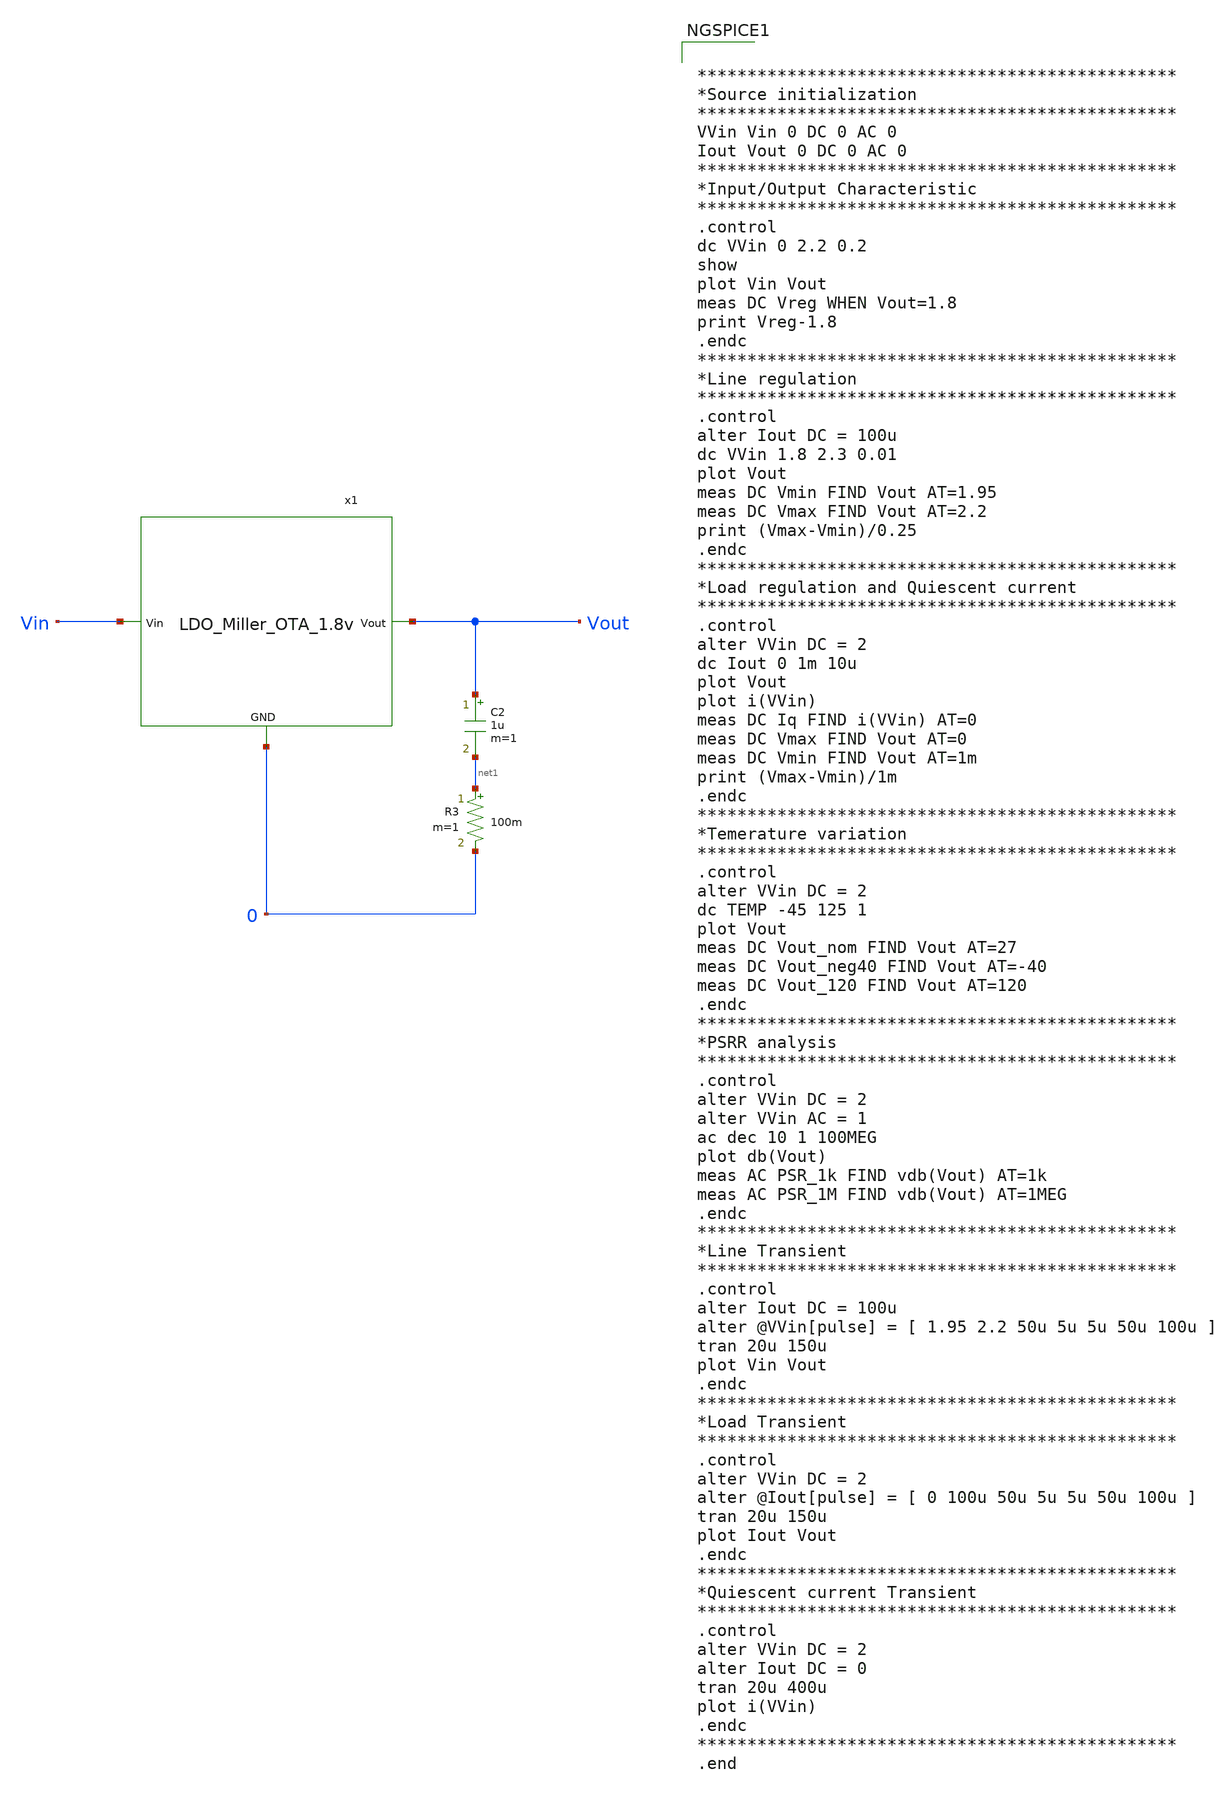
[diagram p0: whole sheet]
** sch_path: Analog_Blocks/LDO/Testbench/LDO_Miller_1.8v_meas.sch
**.subckt LDO_Miller_1.8v_meas
C2 Vout net1 1u m=1
R3 net1 0 100m m=1
x1 Vin Vout 0 LDO_Miller_OTA_1.8v
**** begin user architecture code


************************************************
*Source initialization
************************************************
VVin Vin 0 DC 0 AC 0
Iout Vout 0 DC 0 AC 0
************************************************
*Input/Output Characteristic
************************************************
.control
dc VVin 0 2.2 0.2
show
plot Vin Vout
meas DC Vreg WHEN Vout=1.8
print Vreg-1.8
.endc
************************************************
*Line regulation
************************************************
.control
alter Iout DC = 100u
dc VVin 1.8 2.3 0.01
plot Vout
meas DC Vmin FIND Vout AT=1.95
meas DC Vmax FIND Vout AT=2.2
print (Vmax-Vmin)/0.25
.endc
************************************************
*Load regulation and Quiescent current
************************************************
.control
alter VVin DC = 2
dc Iout 0 1m 10u
plot Vout
plot i(VVin)
meas DC Iq FIND i(VVin) AT=0
meas DC Vmax FIND Vout AT=0
meas DC Vmin FIND Vout AT=1m
print (Vmax-Vmin)/1m
.endc
************************************************
*Temerature variation
************************************************
.control
alter VVin DC = 2
dc TEMP -45 125 1
plot Vout
meas DC Vout_nom FIND Vout AT=27
meas DC Vout_neg40 FIND Vout AT=-40
meas DC Vout_120 FIND Vout AT=120
.endc
************************************************
*PSRR analysis
************************************************
.control
alter VVin DC = 2
alter VVin AC = 1
ac dec 10 1 100MEG
plot db(Vout)
meas AC PSR_1k FIND vdb(Vout) AT=1k
meas AC PSR_1M FIND vdb(Vout) AT=1MEG
.endc
************************************************
*Line Transient
************************************************
.control
alter Iout DC = 100u
alter @VVin[pulse] = [ 1.95 2.2 50u 5u 5u 50u 100u ]
tran 20u 150u
plot Vin Vout
.endc
************************************************
*Load Transient
************************************************
.control
alter VVin DC = 2
alter @Iout[pulse] = [ 0 100u 50u 5u 5u 50u 100u ]
tran 20u 150u
plot Iout Vout
.endc
************************************************
*Quiescent current Transient
************************************************
.control
alter VVin DC = 2
alter Iout DC = 0
tran 20u 400u
plot i(VVin)
.endc
************************************************
.end




.param mc_mm_switch=0
.param mc_pr_switch=0
.include ~/mabrains/Analog_blocks/models/sky130A/libs.ref/sky130_fd_pr/spice/sky130_fd_pr__nfet_01v8__tt.corner.spice
.include ~/mabrains/Analog_blocks/models/sky130A/libs.ref/sky130_fd_pr/spice/sky130_fd_pr__nfet_01v8_lvt__tt.corner.spice
.include ~/mabrains/Analog_blocks/models/sky130A/libs.ref/sky130_fd_pr/spice/sky130_fd_pr__pfet_01v8__tt.corner.spice
.include ~/mabrains/Analog_blocks/models/sky130A/libs.ref/sky130_fd_pr/spice/sky130_fd_pr__nfet_03v3_nvt__tt.corner.spice
.include ~/mabrains/Analog_blocks/models/sky130A/libs.ref/sky130_fd_pr/spice/sky130_fd_pr__nfet_05v0_nvt__tt.corner.spice
.include ~/mabrains/Analog_blocks/models/sky130A/libs.ref/sky130_fd_pr/spice/sky130_fd_pr__esd_nfet_01v8__tt.corner.spice
.include ~/mabrains/Analog_blocks/models/sky130A/libs.ref/sky130_fd_pr/spice/sky130_fd_pr__pfet_01v8_lvt__tt.corner.spice
.include ~/mabrains/Analog_blocks/models/sky130A/libs.ref/sky130_fd_pr/spice/sky130_fd_pr__pfet_01v8_hvt__tt.corner.spice
.include ~/mabrains/Analog_blocks/models/sky130A/libs.ref/sky130_fd_pr/spice/sky130_fd_pr__esd_pfet_g5v0d10v5__tt.corner.spice
.include ~/mabrains/Analog_blocks/models/sky130A/libs.ref/sky130_fd_pr/spice/sky130_fd_pr__pfet_g5v0d10v5__tt.corner.spice
.include ~/mabrains/Analog_blocks/models/sky130A/libs.ref/sky130_fd_pr/spice/sky130_fd_pr__pfet_g5v0d16v0__tt.corner.spice
.include ~/mabrains/Analog_blocks/models/sky130A/libs.ref/sky130_fd_pr/spice/sky130_fd_pr__nfet_g5v0d10v5__tt.corner.spice
.include ~/mabrains/Analog_blocks/models/sky130A/libs.ref/sky130_fd_pr/spice/sky130_fd_pr__nfet_g5v0d16v0__tt_discrete.corner.spice
.include ~/mabrains/Analog_blocks/models/sky130A/libs.ref/sky130_fd_pr/spice/sky130_fd_pr__esd_nfet_g5v0d10v5__tt.corner.spice
.include ~/mabrains/Analog_blocks/models/sky130A/libs.tech/ngspice/corners/tt/nonfet.spice
* Mismatch parameters
.include ~/mabrains/Analog_blocks/models/sky130A/libs.ref/sky130_fd_pr/spice/sky130_fd_pr__nfet_01v8__mismatch.corner.spice
.include ~/mabrains/Analog_blocks/models/sky130A/libs.ref/sky130_fd_pr/spice/sky130_fd_pr__pfet_01v8__mismatch.corner.spice
.include ~/mabrains/Analog_blocks/models/sky130A/libs.ref/sky130_fd_pr/spice/sky130_fd_pr__nfet_01v8_lvt__mismatch.corner.spice
.include ~/mabrains/Analog_blocks/models/sky130A/libs.ref/sky130_fd_pr/spice/sky130_fd_pr__pfet_01v8_lvt__mismatch.corner.spice
.include ~/mabrains/Analog_blocks/models/sky130A/libs.ref/sky130_fd_pr/spice/sky130_fd_pr__pfet_01v8_hvt__mismatch.corner.spice
.include ~/mabrains/Analog_blocks/models/sky130A/libs.ref/sky130_fd_pr/spice/sky130_fd_pr__nfet_g5v0d10v5__mismatch.corner.spice
.include ~/mabrains/Analog_blocks/models/sky130A/libs.ref/sky130_fd_pr/spice/sky130_fd_pr__pfet_g5v0d10v5__mismatch.corner.spice
.include ~/mabrains/Analog_blocks/models/sky130A/libs.ref/sky130_fd_pr/spice/sky130_fd_pr__nfet_05v0_nvt__mismatch.corner.spice
.include ~/mabrains/Analog_blocks/models/sky130A/libs.ref/sky130_fd_pr/spice/sky130_fd_pr__nfet_03v3_nvt__mismatch.corner.spice
* Resistor/Capacitor
.include ~/mabrains/Analog_blocks/models/sky130A/libs.tech/ngspice/r+c/res_typical__cap_typical.spice
.include ~/mabrains/Analog_blocks/models/sky130A/libs.tech/ngspice/r+c/res_typical__cap_typical__lin.spice
* Special cells
.include ~/mabrains/Analog_blocks/models/sky130A/libs.tech/ngspice/corners/tt/specialized_cells.spice
* All models
.include ~/mabrains/Analog_blocks/models/sky130A/libs.tech/ngspice/all.spice
* Corner
.include ~/mabrains/Analog_blocks/models/sky130A/libs.tech/ngspice/corners/tt/rf.spice



**** end user architecture code
**.ends
.end
